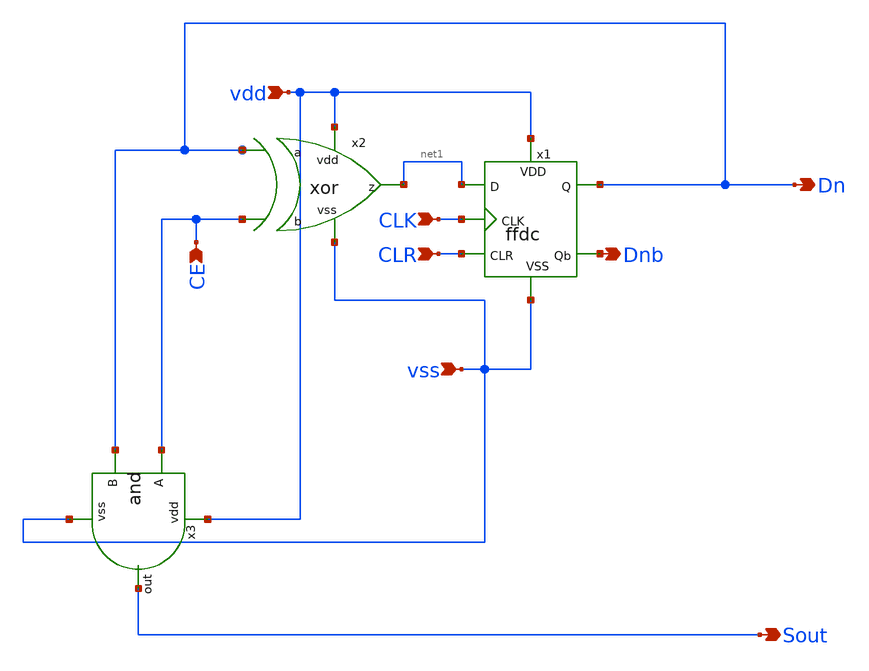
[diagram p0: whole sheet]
** sch_path: track_vlsi/ledesma/sch/bitc.sch
**.subckt bitc Dn Sout vdd vss CLK CLR CE Dnb
*.opin Dn
*.opin Sout
*.ipin vdd
*.ipin vss
*.ipin CLK
*.ipin CLR
*.ipin CE
*.opin Dnb
x2 vdd Dn CE net1 vss xor
x3 vdd CE Dn Sout vss and
x1 vdd vss Dn net1 CLK CLR Dnb ffdc
**.ends
.end
